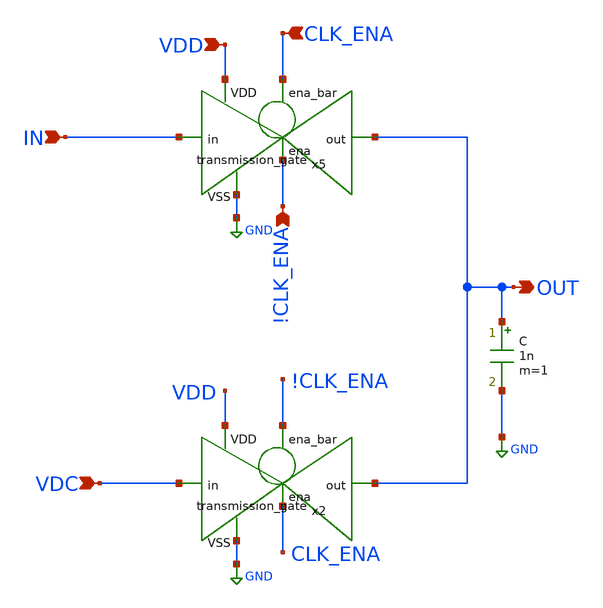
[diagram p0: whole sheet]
** sch_path: designs/libs/core_amps/start_up_cir/start_up_cir_cap.sch
**.subckt start_up_cir_cap IN OUT VDC VDD CLK_ENA !CLK_ENA
*.ipin IN
*.opin OUT
*.ipin VDC
*.ipin VDD
*.ipin CLK_ENA
*.ipin !CLK_ENA
x2 !CLK_ENA VDD OUT VDC GND CLK_ENA transmission_gate
x5 CLK_ENA VDD OUT IN GND !CLK_ENA transmission_gate
C OUT GND 1n m=1
**.ends

* expanding   symbol:  libs/core_digital/schem/transmission_gate.sym # of pins=6
** sym_path: designs/libs/core_digital/schem/transmission_gate.sym
** sch_path: designs/libs/core_digital/schem/transmission_gate.sch
.subckt transmission_gate ena_bar VDD out in VSS ena
*.ipin in
*.ipin ena_bar
*.ipin ena
*.ipin VSS
*.ipin VDD
*.opin out
XM1 in ena_bar out VDD pfet_03v3 L=0.28u W=0.22u nf=1 ad='int((nf+1)/2) * W/nf * 0.18u' as='int((nf+2)/2) * W/nf * 0.18u'
+ pd='2*int((nf+1)/2) * (W/nf + 0.18u)' ps='2*int((nf+2)/2) * (W/nf + 0.18u)' nrd='0.18u / W' nrs='0.18u / W'
+ sa=0 sb=0 sd=0 m=1
XM2 in ena out VSS nfet_03v3 L=0.28u W=0.22u nf=1 ad='int((nf+1)/2) * W/nf * 0.18u' as='int((nf+2)/2) * W/nf * 0.18u'
+ pd='2*int((nf+1)/2) * (W/nf + 0.18u)' ps='2*int((nf+2)/2) * (W/nf + 0.18u)' nrd='0.18u / W' nrs='0.18u / W'
+ sa=0 sb=0 sd=0 m=1
.ends

.GLOBAL GND
.end
